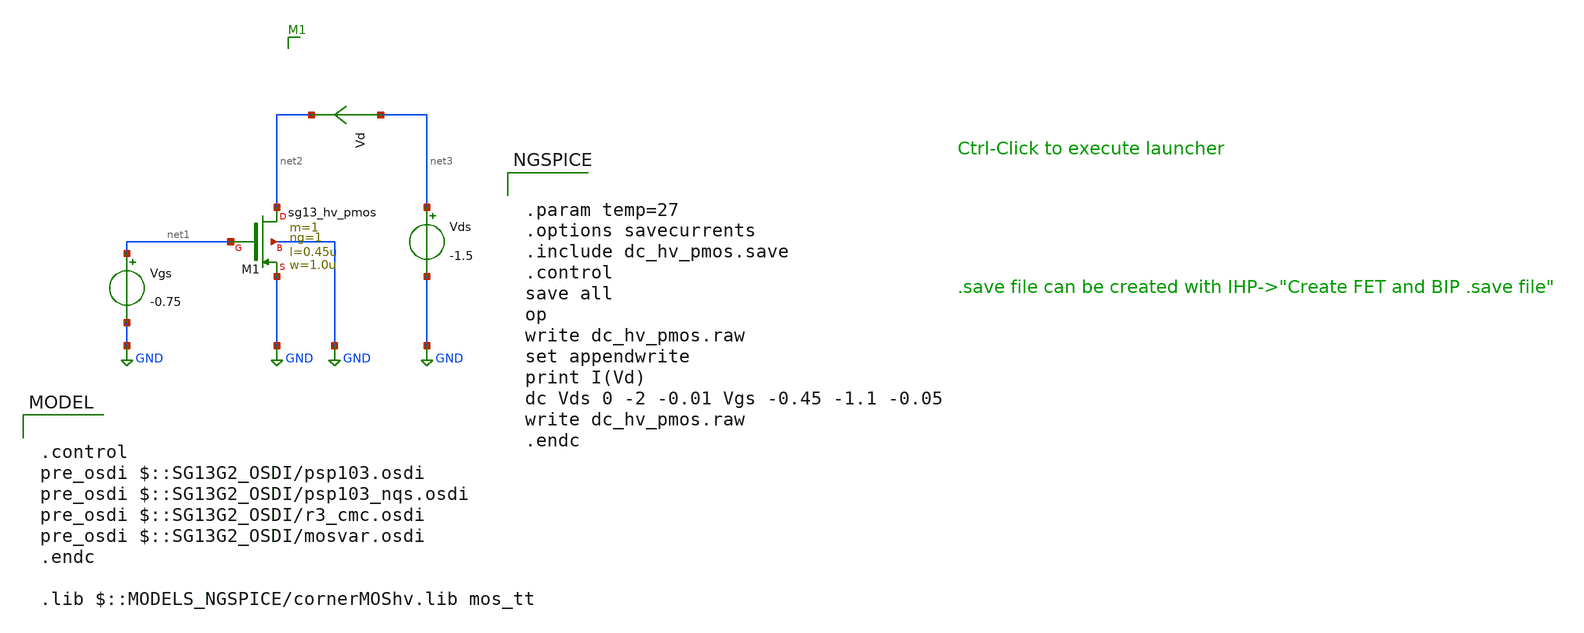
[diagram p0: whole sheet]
** sch_path: ihp-sg13g2/xschem_libs/sg13g2_tests/dc_hv_pmos/schematic/dc_hv_pmos.sch
* Copyright 2023 IHP PDK Authors
**.subckt dc_hv_pmos
Vgs net1 GND -0.75
Vds net3 GND -1.5
XM1 net2 net1 GND GND sg13_hv_pmos w=1.0u l=0.45u ng=1 m=1 mm_ok=1
Vd net3 net2 0
.save i(vd)
**** begin user architecture code

.control
pre_osdi $::SG13G2_OSDI/psp103.osdi
pre_osdi $::SG13G2_OSDI/psp103_nqs.osdi
pre_osdi $::SG13G2_OSDI/r3_cmc.osdi
pre_osdi $::SG13G2_OSDI/mosvar.osdi
.endc

.lib $::MODELS_NGSPICE/cornerMOShv.lib mos_tt



.param temp=27
.options savecurrents
.include dc_hv_pmos.save
.control
save all
op
write dc_hv_pmos.raw
set appendwrite
print I(Vd)
dc Vds 0 -2 -0.01 Vgs -0.45 -1.1 -0.05
write dc_hv_pmos.raw
.endc


**** end user architecture code
**.ends
.GLOBAL GND
.end
